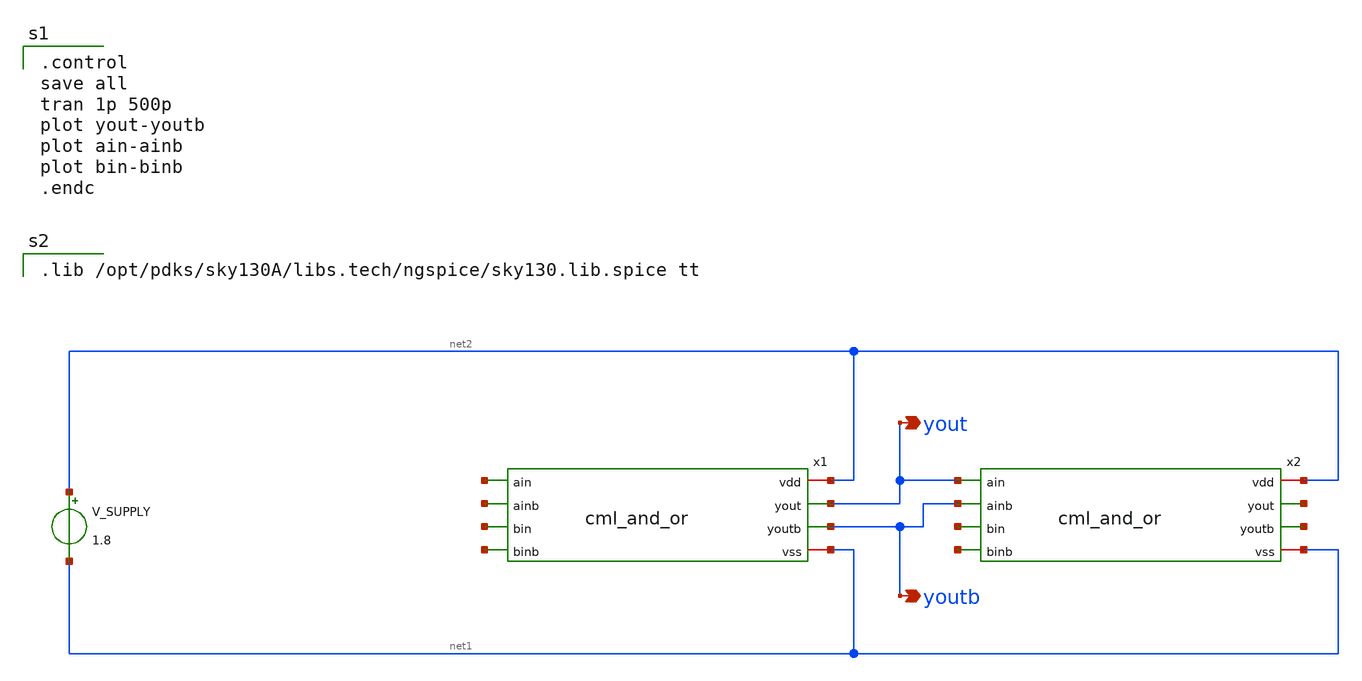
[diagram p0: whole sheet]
** sch_path: xschem/cml_and_or_tb.sch
**.subckt cml_and_or_tb youtb yout
*.opin youtb
*.opin yout
x1 net2 yout youtb net3 net4 net5 net6 net1 cml_and_or
V_SUPPLY net2 net1 1.8
x2 net2 net7 net8 yout youtb net9 net10 net1 cml_and_or
**** begin user architecture code

.lib /opt/pdks/sky130A/libs.tech/ngspice/sky130.lib.spice tt


.control
save all
tran 1p 500p
plot yout-youtb
plot ain-ainb
plot bin-binb
.endc

**** end user architecture code
**.ends

* expanding   symbol:  cml_and_or.sym # of pins=8
** sym_path: xschem/cml_and_or.sym
** sch_path: xschem/cml_and_or.sch
.subckt cml_and_or vdd yout youtb ain ainb bin binb vss
*.ipin ain
*.ipin ainb
*.ipin binb
*.ipin bin
*.opin yout
*.opin youtb
*.iopin vdd
*.iopin vss
XM1 youtb ain net1 vss sky130_fd_pr__nfet_01v8 L=0.15 W=18 nf=1 ad='int((nf+1)/2) * W/nf * 0.29' as='int((nf+2)/2) * W/nf * 0.29'
+ pd='2*int((nf+1)/2) * (W/nf + 0.29)' ps='2*int((nf+2)/2) * (W/nf + 0.29)' nrd='0.29 / W' nrs='0.29 / W'
+ sa=0 sb=0 sd=0 mult=1 m=1
XM2 yout ainb net1 vss sky130_fd_pr__nfet_01v8 L=0.15 W=18 nf=1 ad='int((nf+1)/2) * W/nf * 0.29' as='int((nf+2)/2) * W/nf * 0.29'
+ pd='2*int((nf+1)/2) * (W/nf + 0.29)' ps='2*int((nf+2)/2) * (W/nf + 0.29)' nrd='0.29 / W' nrs='0.29 / W'
+ sa=0 sb=0 sd=0 mult=1 m=1
XM3 net1 bin net2 vss sky130_fd_pr__nfet_01v8 L=0.15 W=18 nf=1 ad='int((nf+1)/2) * W/nf * 0.29' as='int((nf+2)/2) * W/nf * 0.29'
+ pd='2*int((nf+1)/2) * (W/nf + 0.29)' ps='2*int((nf+2)/2) * (W/nf + 0.29)' nrd='0.29 / W' nrs='0.29 / W'
+ sa=0 sb=0 sd=0 mult=1 m=1
XM4 yout binb net2 vss sky130_fd_pr__nfet_01v8 L=0.15 W=18 nf=1 ad='int((nf+1)/2) * W/nf * 0.29' as='int((nf+2)/2) * W/nf * 0.29'
+ pd='2*int((nf+1)/2) * (W/nf + 0.29)' ps='2*int((nf+2)/2) * (W/nf + 0.29)' nrd='0.29 / W' nrs='0.29 / W'
+ sa=0 sb=0 sd=0 mult=1 m=1
R1 vdd youtb 300 m=1
R2 vdd yout 300 m=1
I0 net2 vss 1m
.ends

.end
